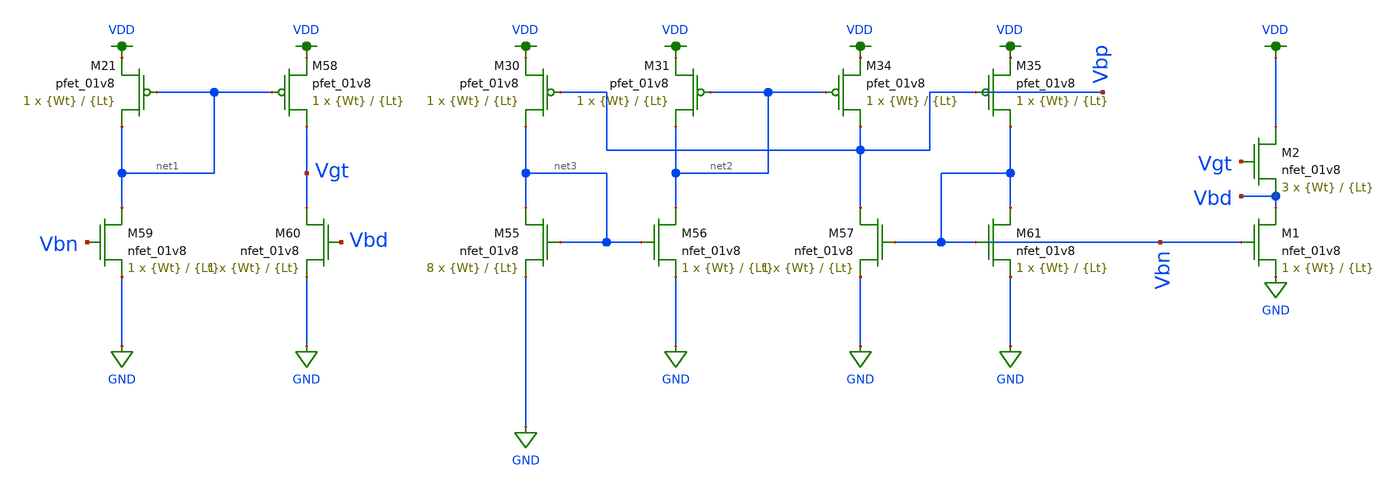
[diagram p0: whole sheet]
** sch_path: schematic/LDS/test/ibias_vgt_oglvs.sch
**.subckt ibias_vgt_oglvs
XM1 Vbd Vbn GND GND sky130_fd_pr__nfet_01v8 L={Lt} W={Wt} nf=1 ad='int((nf+1)/2) * W/nf * 0.29' as='int((nf+2)/2) * W/nf * 0.29'
+ pd='2*int((nf+1)/2) * (W/nf + 0.29)' ps='2*int((nf+2)/2) * (W/nf + 0.29)' nrd='0.29 / W' nrs='0.29 / W'
+ sa=0 sb=0 sd=0 mult=1 m=1
XM2 VDD Vgt Vbd GND sky130_fd_pr__nfet_01v8 L={Lt} W={Wt} nf=1 ad='int((nf+1)/2) * W/nf * 0.29' as='int((nf+2)/2) * W/nf * 0.29'
+ pd='2*int((nf+1)/2) * (W/nf + 0.29)' ps='2*int((nf+2)/2) * (W/nf + 0.29)' nrd='0.29 / W' nrs='0.29 / W'
+ sa=0 sb=0 sd=0 mult=3 m=3
XM21 net1 net1 VDD VDD sky130_fd_pr__pfet_01v8 L={Lt} W={Wt} nf=1 ad='int((nf+1)/2) * W/nf * 0.29' as='int((nf+2)/2) * W/nf * 0.29'
+ pd='2*int((nf+1)/2) * (W/nf + 0.29)' ps='2*int((nf+2)/2) * (W/nf + 0.29)' nrd='0.29 / W' nrs='0.29 / W'
+ sa=0 sb=0 sd=0 mult=1 m=1
XM58 Vgt net1 VDD VDD sky130_fd_pr__pfet_01v8 L={Lt} W={Wt} nf=1 ad='int((nf+1)/2) * W/nf * 0.29' as='int((nf+2)/2) * W/nf * 0.29'
+ pd='2*int((nf+1)/2) * (W/nf + 0.29)' ps='2*int((nf+2)/2) * (W/nf + 0.29)' nrd='0.29 / W' nrs='0.29 / W'
+ sa=0 sb=0 sd=0 mult=1 m=1
XM59 net1 Vbn GND GND sky130_fd_pr__nfet_01v8 L={Lt} W={Wt} nf=1 ad='int((nf+1)/2) * W/nf * 0.29' as='int((nf+2)/2) * W/nf * 0.29'
+ pd='2*int((nf+1)/2) * (W/nf + 0.29)' ps='2*int((nf+2)/2) * (W/nf + 0.29)' nrd='0.29 / W' nrs='0.29 / W'
+ sa=0 sb=0 sd=0 mult=1 m=1
XM60 Vgt Vbd GND GND sky130_fd_pr__nfet_01v8 L={Lt} W={Wt} nf=1 ad='int((nf+1)/2) * W/nf * 0.29' as='int((nf+2)/2) * W/nf * 0.29'
+ pd='2*int((nf+1)/2) * (W/nf + 0.29)' ps='2*int((nf+2)/2) * (W/nf + 0.29)' nrd='0.29 / W' nrs='0.29 / W'
+ sa=0 sb=0 sd=0 mult=1 m=1
XM30 net3 Vbp VDD VDD sky130_fd_pr__pfet_01v8 L={Lt} W={Wt} nf=1 ad='int((nf+1)/2) * W/nf * 0.29' as='int((nf+2)/2) * W/nf * 0.29'
+ pd='2*int((nf+1)/2) * (W/nf + 0.29)' ps='2*int((nf+2)/2) * (W/nf + 0.29)' nrd='0.29 / W' nrs='0.29 / W'
+ sa=0 sb=0 sd=0 mult=1 m=1
XM31 net2 net2 VDD VDD sky130_fd_pr__pfet_01v8 L={Lt} W={Wt} nf=1 ad='int((nf+1)/2) * W/nf * 0.29' as='int((nf+2)/2) * W/nf * 0.29'
+ pd='2*int((nf+1)/2) * (W/nf + 0.29)' ps='2*int((nf+2)/2) * (W/nf + 0.29)' nrd='0.29 / W' nrs='0.29 / W'
+ sa=0 sb=0 sd=0 mult=1 m=1
XM34 Vbp net2 VDD VDD sky130_fd_pr__pfet_01v8 L={Lt} W={Wt} nf=1 ad='int((nf+1)/2) * W/nf * 0.29' as='int((nf+2)/2) * W/nf * 0.29'
+ pd='2*int((nf+1)/2) * (W/nf + 0.29)' ps='2*int((nf+2)/2) * (W/nf + 0.29)' nrd='0.29 / W' nrs='0.29 / W'
+ sa=0 sb=0 sd=0 mult=1 m=1
XM35 Vbn Vbp VDD VDD sky130_fd_pr__pfet_01v8 L={Lt} W={Wt} nf=1 ad='int((nf+1)/2) * W/nf * 0.29' as='int((nf+2)/2) * W/nf * 0.29'
+ pd='2*int((nf+1)/2) * (W/nf + 0.29)' ps='2*int((nf+2)/2) * (W/nf + 0.29)' nrd='0.29 / W' nrs='0.29 / W'
+ sa=0 sb=0 sd=0 mult=1 m=1
XM55 net3 net3 GND GND sky130_fd_pr__nfet_01v8 L={Lt} W={Wt} nf=1 ad='int((nf+1)/2) * W/nf * 0.29' as='int((nf+2)/2) * W/nf * 0.29'
+ pd='2*int((nf+1)/2) * (W/nf + 0.29)' ps='2*int((nf+2)/2) * (W/nf + 0.29)' nrd='0.29 / W' nrs='0.29 / W'
+ sa=0 sb=0 sd=0 mult=8 m=8
XM56 net2 net3 GND GND sky130_fd_pr__nfet_01v8 L={Lt} W={Wt} nf=1 ad='int((nf+1)/2) * W/nf * 0.29' as='int((nf+2)/2) * W/nf * 0.29'
+ pd='2*int((nf+1)/2) * (W/nf + 0.29)' ps='2*int((nf+2)/2) * (W/nf + 0.29)' nrd='0.29 / W' nrs='0.29 / W'
+ sa=0 sb=0 sd=0 mult=1 m=1
XM57 Vbp Vbn GND GND sky130_fd_pr__nfet_01v8 L={Lt} W={Wt} nf=1 ad='int((nf+1)/2) * W/nf * 0.29' as='int((nf+2)/2) * W/nf * 0.29'
+ pd='2*int((nf+1)/2) * (W/nf + 0.29)' ps='2*int((nf+2)/2) * (W/nf + 0.29)' nrd='0.29 / W' nrs='0.29 / W'
+ sa=0 sb=0 sd=0 mult=1 m=1
XM61 Vbn Vbn GND GND sky130_fd_pr__nfet_01v8 L={Lt} W={Wt} nf=1 ad='int((nf+1)/2) * W/nf * 0.29' as='int((nf+2)/2) * W/nf * 0.29'
+ pd='2*int((nf+1)/2) * (W/nf + 0.29)' ps='2*int((nf+2)/2) * (W/nf + 0.29)' nrd='0.29 / W' nrs='0.29 / W'
+ sa=0 sb=0 sd=0 mult=1 m=1
**.ends
.GLOBAL GND
.GLOBAL VDD
.end
